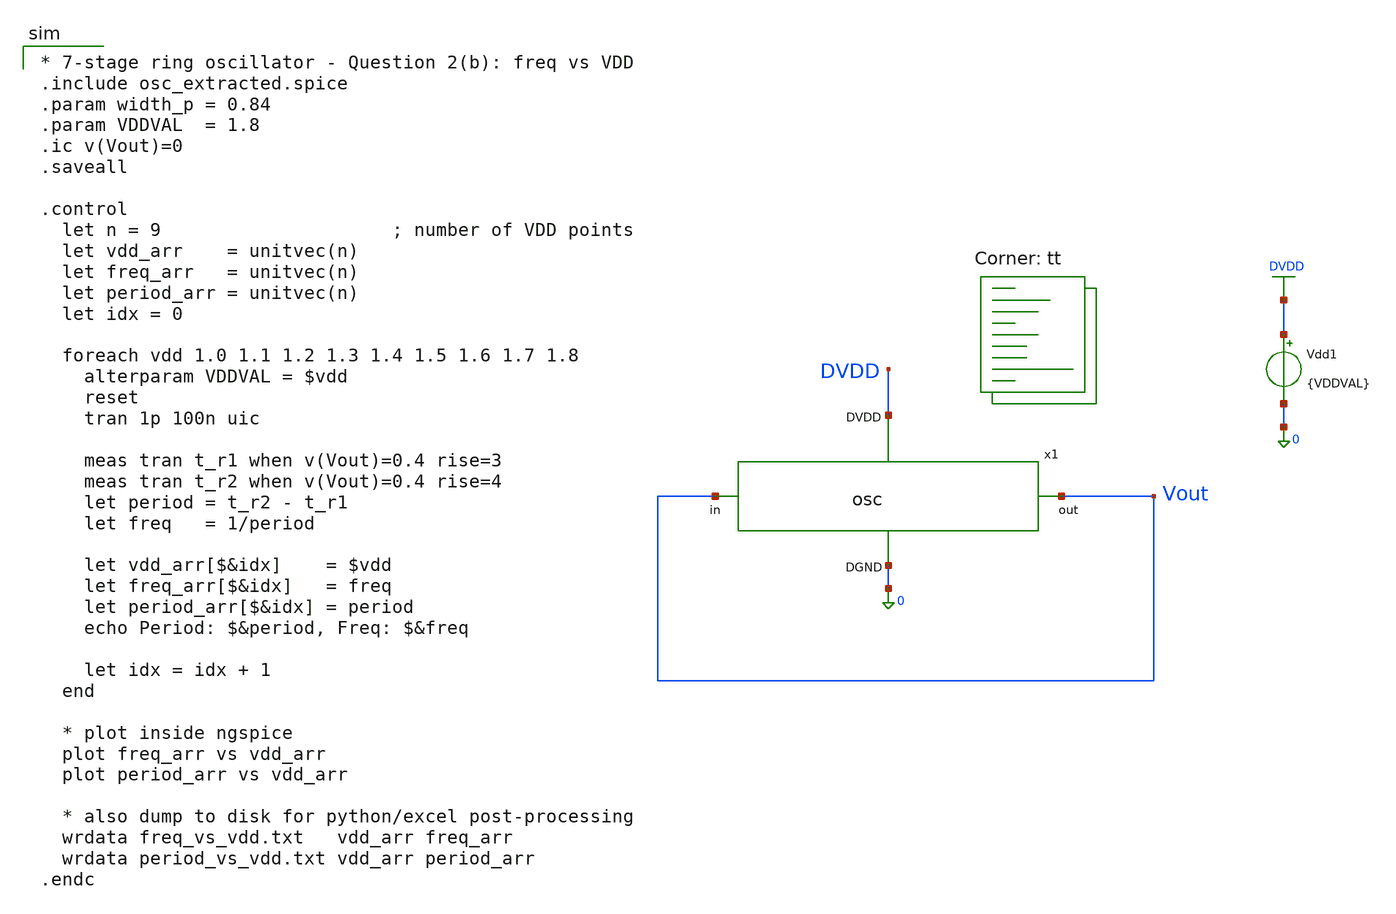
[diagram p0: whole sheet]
** sch_path: tutorial-4/source/q2/q2.sch
**.subckt q2
Vdd1 DVDD 0 {VDDVAL}
x1 DVDD Vout Vout 0 osc
**** begin user architecture code

* 7-stage ring oscillator - Question 2(b): freq vs VDD
.include osc_extracted.spice
.param width_p = 0.84
.param VDDVAL  = 1.8
.ic v(Vout)=0
.saveall

.control
  let n = 9                     ; number of VDD points
  let vdd_arr    = unitvec(n)
  let freq_arr   = unitvec(n)
  let period_arr = unitvec(n)
  let idx = 0

  foreach vdd 1.0 1.1 1.2 1.3 1.4 1.5 1.6 1.7 1.8
    alterparam VDDVAL = $vdd
    reset
    tran 1p 100n uic

    meas tran t_r1 when v(Vout)=0.4 rise=3
    meas tran t_r2 when v(Vout)=0.4 rise=4
    let period = t_r2 - t_r1
    let freq   = 1/period

    let vdd_arr[$&idx]    = $vdd
    let freq_arr[$&idx]   = freq
    let period_arr[$&idx] = period
    echo Period: $&period, Freq: $&freq

    let idx = idx + 1
  end

  * plot inside ngspice
  plot freq_arr vs vdd_arr
  plot period_arr vs vdd_arr

  * also dump to disk for python/excel post-processing
  wrdata freq_vs_vdd.txt   vdd_arr freq_arr
  wrdata period_vs_vdd.txt vdd_arr period_arr
.endc

.lib $::SKYWATER_MODELS/sky130.lib.spice tt
**** end user architecture code
**.ends
.GLOBAL DVDD
.end
